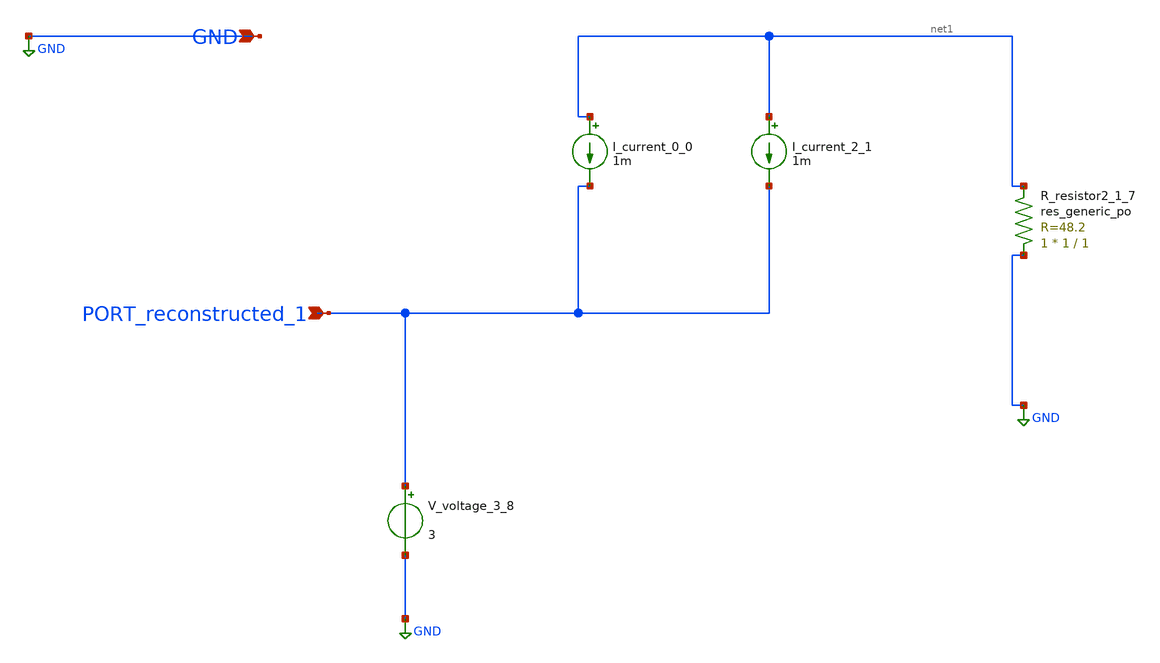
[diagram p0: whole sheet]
** sch_path: schematics/AMSNet/76.sch
**.subckt 76 PORT_reconstructed_1 GND
*.ipin PORT_reconstructed_1
*.ipin GND
I_current_0_0 net1 PORT_reconstructed_1 1m
I_current_2_1 net1 PORT_reconstructed_1 1m
XR_resistor2_1_7 GND net1 sky130_fd_pr__res_generic_po W=1 L=1 m=1
V_voltage_3_8 PORT_reconstructed_1 GND 3
**.ends
.GLOBAL GND
.end
